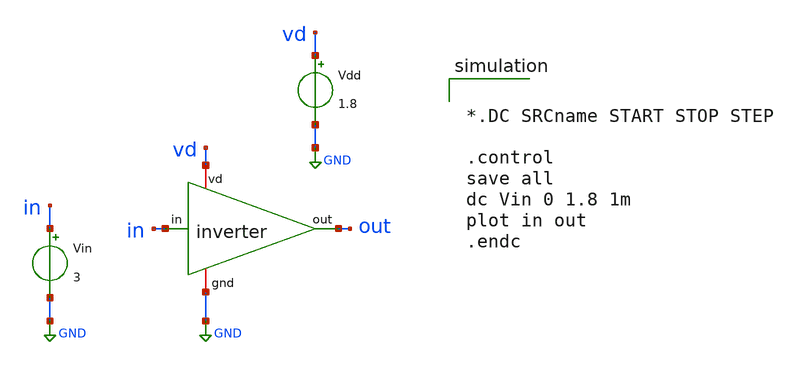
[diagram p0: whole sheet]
** sch_path: xschem_files/inverter_tb-dc.sch
**.subckt inverter_tb-dc
x1 vd in out GND inverter
Vin in GND 3
Vdd vd GND 1.8
**** begin user architecture code


*.DC SRCname START STOP STEP

.control
save all
dc Vin 0 1.8 1m
plot in out
.endc




** opencircuitdesign pdks install
.lib $::SKYWATER_MODELS/sky130.lib.spice tt


**** end user architecture code
**.ends

* expanding   symbol:  inverter.sym # of pins=4
** sym_path: xschem_files/inverter.sym
** sch_path: xschem_files/inverter.sch
.subckt inverter vd in out gnd
*.ipin in
*.opin out
*.iopin vd
*.iopin gnd
XN0 out in gnd gnd sky130_fd_pr__nfet_01v8 L=0.15 W=1 nf=1 ad='int((nf+1)/2) * W/nf * 0.29' as='int((nf+2)/2) * W/nf * 0.29'
+ pd='2*int((nf+1)/2) * (W/nf + 0.29)' ps='2*int((nf+2)/2) * (W/nf + 0.29)' nrd='0.29 / W' nrs='0.29 / W'
+ sa=0 sb=0 sd=0 mult=1 m=1
XP0 out in vd vd sky130_fd_pr__pfet_01v8 L=0.15 W=3 nf=1 ad='int((nf+1)/2) * W/nf * 0.29' as='int((nf+2)/2) * W/nf * 0.29'
+ pd='2*int((nf+1)/2) * (W/nf + 0.29)' ps='2*int((nf+2)/2) * (W/nf + 0.29)' nrd='0.29 / W' nrs='0.29 / W'
+ sa=0 sb=0 sd=0 mult=1 m=1
.ends

.GLOBAL GND
.end
